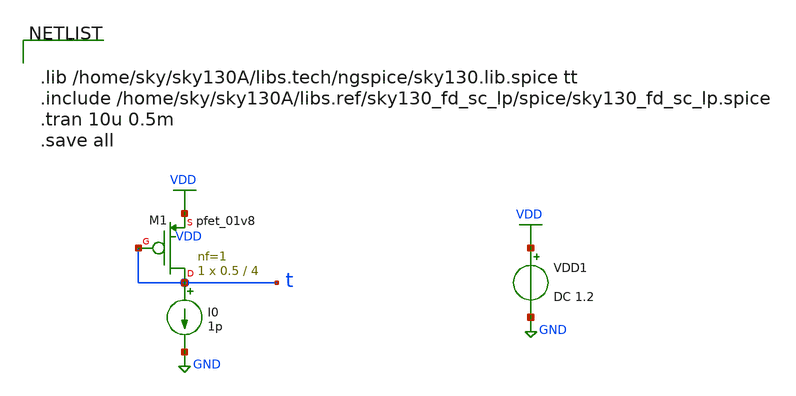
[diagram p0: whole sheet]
** sch_path: xschem/comparator_latest/archive/biasingTest.sch
**.subckt biasingTest
VDD1 VDD GND DC 1.2
I0 t GND 1p
XM1 t t VDD VDD sky130_fd_pr__pfet_01v8 L=4 W=0.5 nf=1 ad='int((nf+1)/2) * W/nf * 0.29' as='int((nf+2)/2) * W/nf * 0.29'
+ pd='2*int((nf+1)/2) * (W/nf + 0.29)' ps='2*int((nf+2)/2) * (W/nf + 0.29)' nrd='0.29 / W' nrs='0.29 / W'
+ sa=0 sb=0 sd=0 mult=1 m=1
**** begin user architecture code


.lib /home/sky/sky130A/libs.tech/ngspice/sky130.lib.spice tt
.include /home/sky/sky130A/libs.ref/sky130_fd_sc_lp/spice/sky130_fd_sc_lp.spice
.tran 10u 0.5m
.save all


**** end user architecture code
**.ends
.GLOBAL GND
.GLOBAL VDD
.end
